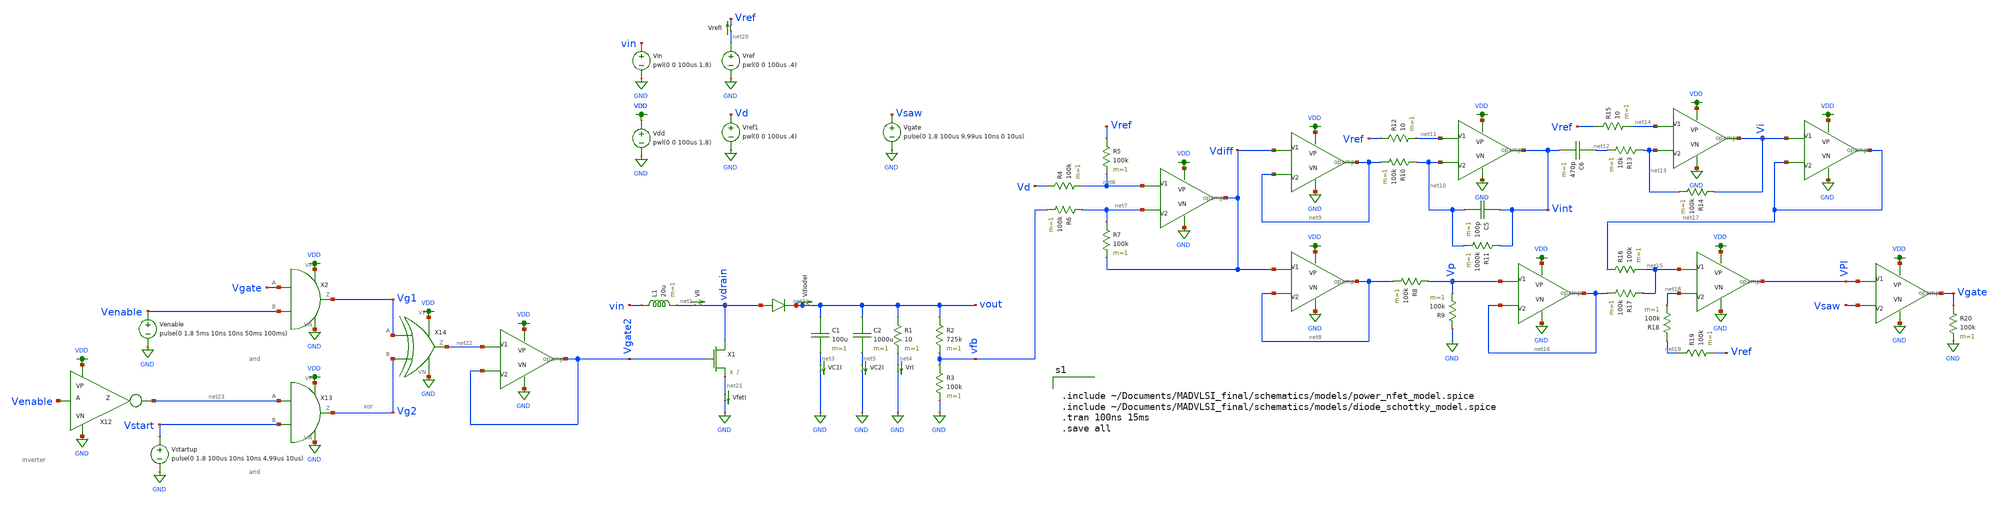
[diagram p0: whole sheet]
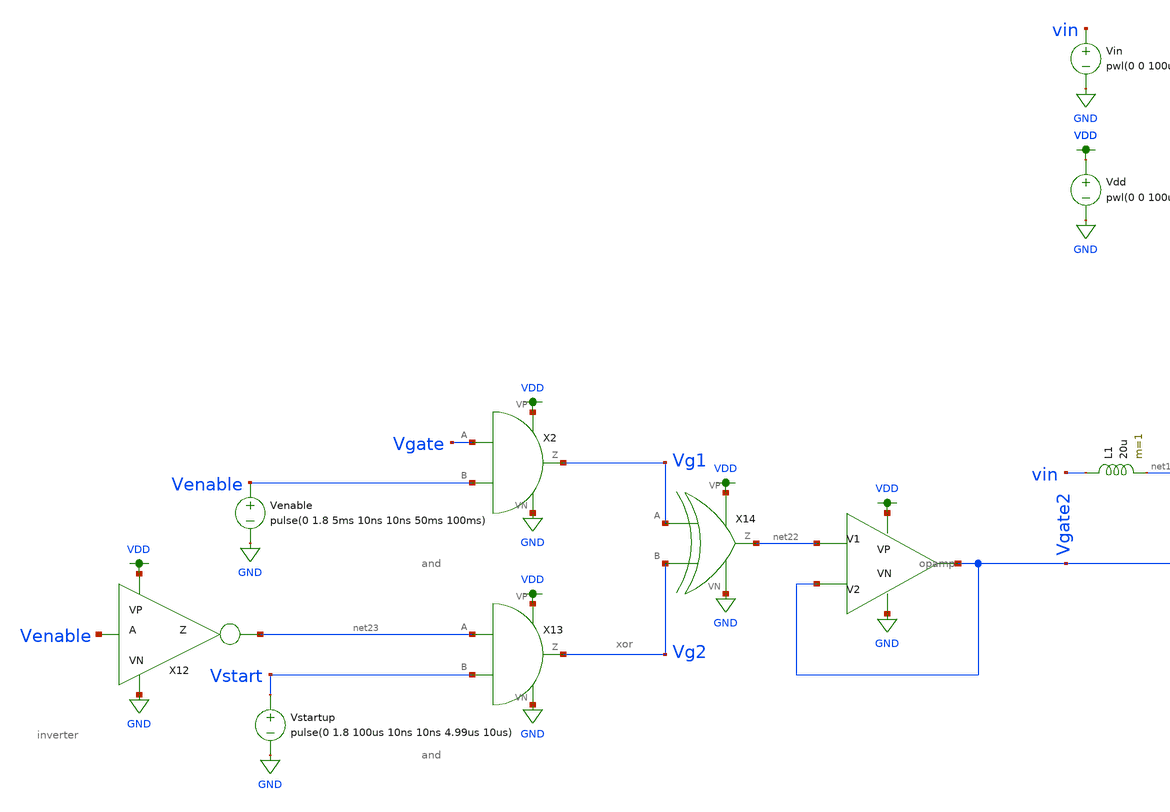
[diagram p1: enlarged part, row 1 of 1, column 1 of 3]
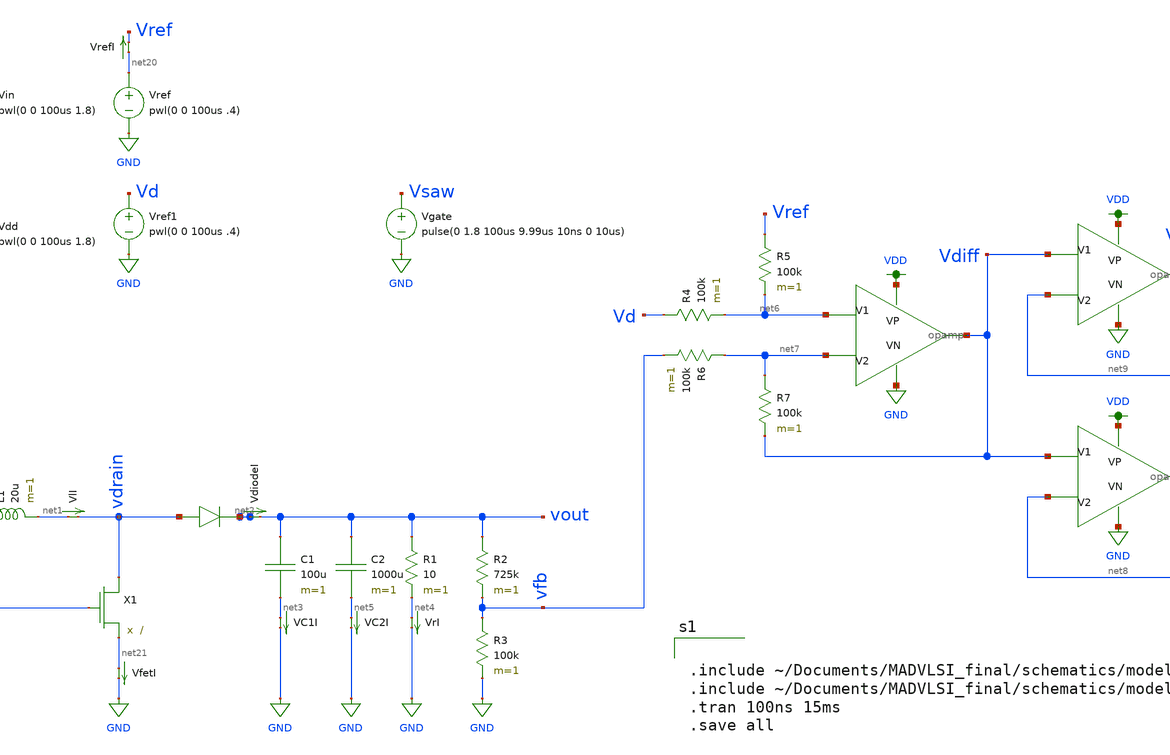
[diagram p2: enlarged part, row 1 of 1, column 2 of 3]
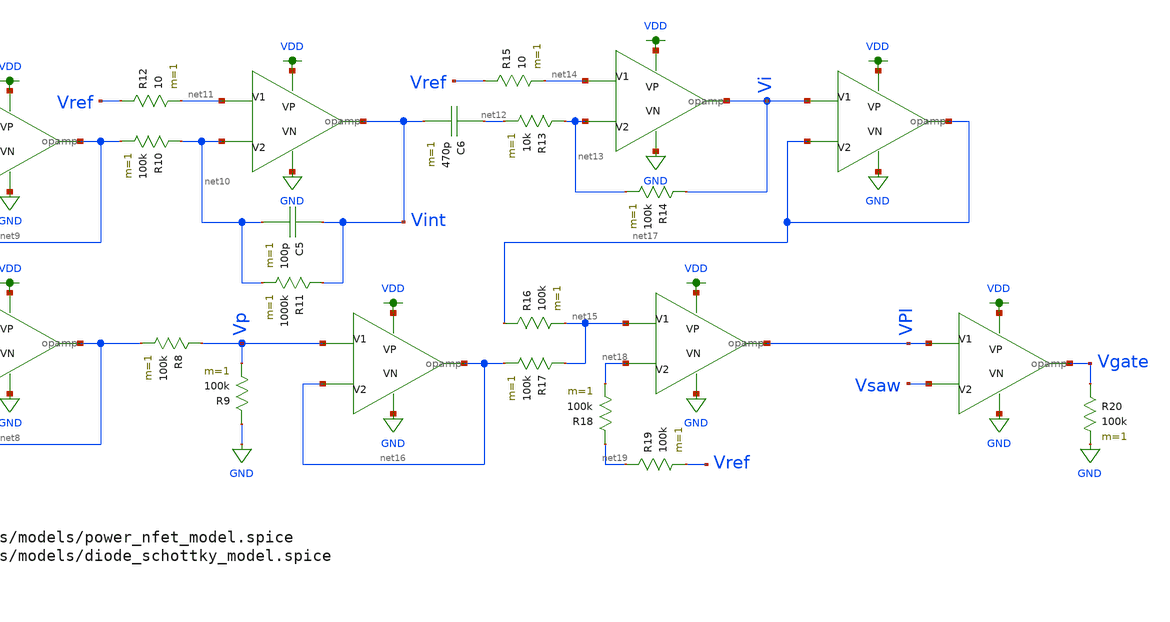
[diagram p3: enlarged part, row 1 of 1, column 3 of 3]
** sch_path: schematics/boost_VMC.sch
**.subckt boost_VMC
Vin vin GND pwl(0 0 100us 1.8)
VfetI net21 GND 0
.save i(vfeti)
X1 vdrain Vgate2 net21 power_nfet
L1 vin net1 20u m=1
D1 vdrain net2 diode_schottky
C1 vout net3 100u m=1
R1 vout net4 10 m=1
VlI net1 vdrain 0
.save i(vli)
VdiodeI net2 vout 0
.save i(vdiodei)
VC1I net3 GND 0
.save i(vc1i)
VrI net4 GND 0
.save i(vri)
C2 vout net5 1000u m=1
VC2I net5 GND 0
.save i(vc2i)
R2 vout vfb 725k m=1
R3 vfb GND 100k m=1
Vdd VDD GND pwl(0 0 100us 1.8)
Vref net20 GND pwl(0 0 100us .4)
R4 Vd net6 100k m=1
Vref1 Vd GND pwl(0 0 100us .4)
R5 Vref net6 100k m=1
R6 net7 vfb 100k m=1
R7 net7 Vdiff 100k m=1
X3 net6 net7 VDD GND Vdiff opamp
X4 Vdiff net8 VDD GND net8 opamp
X5 Vdiff net9 VDD GND net9 opamp
R8 Vp net8 100k m=1
R9 GND Vp 100k m=1
X6 net11 net10 VDD GND Vint opamp
R10 net10 net9 100k m=1
C5 Vint net10 100p m=1
R11 Vint net10 1000k m=1
R12 Vref net11 10 m=1
X7 net14 net13 VDD GND Vi opamp
C6 net12 Vint 470p m=1
R13 net13 net12 10k m=1
R14 Vi net13 100k m=1
R15 Vref net14 10 m=1
X8 net15 net18 VDD GND VPI opamp
R16 net17 net15 100k m=1
R17 net15 net16 100k m=1
X9 Vp net16 VDD GND net16 opamp
X10 Vi net17 VDD GND net17 opamp
R18 net19 net18 100k m=1
R19 net19 Vref 100k m=1
X11 VPI Vsaw VDD GND Vgate opamp
Vgate Vsaw GND pulse(0 1.8 100us 9.99us 10ns 0 10us)
VrefI net20 Vref 0
.save i(vrefi)
X2 Vgate Venable VDD GND Vg1 and
X12 Venable VDD GND net23 inverter
Venable Venable GND pulse(0 1.8 5ms 10ns 10ns 50ms 100ms)
R20 Vgate GND 100k m=1
X13 net23 Vstart VDD GND Vg2 and
Vstartup Vstart GND pulse(0 1.8 100us 10ns 10ns 4.99us 10us)
X14 Vg1 Vg2 VDD GND net22 xor
X15 net22 Vgate2 VDD GND Vgate2 opamp
**** begin user architecture code


.include ~/Documents/MADVLSI_final/schematics/models/power_nfet_model.spice
.include ~/Documents/MADVLSI_final/schematics/models/diode_schottky_model.spice
.tran 100ns 15ms
.save all


.option wnflag=1
.lib ~/skywater/skywater-pdk/libraries/sky130_fd_pr_ngspice/latest/models/sky130.lib.spice tt

**** end user architecture code
**.ends

* expanding   symbol:  /home/madvlsi/Documents/MADVLSI_final/schematics/opamp.sym # of pins=5
** sym_path: schematics/opamp.sym
** sch_path: schematics/opamp.sch
.subckt opamp V1 V2 VP VN Vout
*.ipin V1
*.ipin V2
*.opin Vout
*.iopin VP
*.iopin VN
*.iopin VP
*.iopin VN
XM1 VN net7 net2 GND sky130_fd_pr__nfet_01v8 L=l W=w nf=1 ad='int((nf+1)/2) * W/nf * 0.29' as='int((nf+2)/2) * W/nf * 0.29'
+ pd='2*int((nf+1)/2) * (W/nf + 0.29)' ps='2*int((nf+2)/2) * (W/nf + 0.29)' nrd='0.29 / W' nrs='0.29 / W'
+ sa=0 sb=0 sd=0 mult=1 m=1
XM2 VP net3 net1 VDD sky130_fd_pr__pfet_01v8 L=l W=w nf=1 ad='int((nf+1)/2) * W/nf * 0.29' as='int((nf+2)/2) * W/nf * 0.29'
+ pd='2*int((nf+1)/2) * (W/nf + 0.29)' ps='2*int((nf+2)/2) * (W/nf + 0.29)' nrd='0.29 / W' nrs='0.29 / W'
+ sa=0 sb=0 sd=0 mult=1 m=1
XM3 net1 V1 Vd VDD sky130_fd_pr__pfet_01v8 L=l W=w nf=1 ad='int((nf+1)/2) * W/nf * 0.29' as='int((nf+2)/2) * W/nf * 0.29'
+ pd='2*int((nf+1)/2) * (W/nf + 0.29)' ps='2*int((nf+2)/2) * (W/nf + 0.29)' nrd='0.29 / W' nrs='0.29 / W'
+ sa=0 sb=0 sd=0 mult=1 m=1
XM4 Vc V2 net1 VDD sky130_fd_pr__pfet_01v8 L=l W=w nf=1 ad='int((nf+1)/2) * W/nf * 0.29' as='int((nf+2)/2) * W/nf * 0.29'
+ pd='2*int((nf+1)/2) * (W/nf + 0.29)' ps='2*int((nf+2)/2) * (W/nf + 0.29)' nrd='0.29 / W' nrs='0.29 / W'
+ sa=0 sb=0 sd=0 mult=1 m=1
XM5 Va V2 net2 GND sky130_fd_pr__nfet_01v8 L=l W=w nf=1 ad='int((nf+1)/2) * W/nf * 0.29' as='int((nf+2)/2) * W/nf * 0.29'
+ pd='2*int((nf+1)/2) * (W/nf + 0.29)' ps='2*int((nf+2)/2) * (W/nf + 0.29)' nrd='0.29 / W' nrs='0.29 / W'
+ sa=0 sb=0 sd=0 mult=1 m=1
XM6 net2 V1 Vb GND sky130_fd_pr__nfet_01v8 L=l W=w nf=1 ad='int((nf+1)/2) * W/nf * 0.29' as='int((nf+2)/2) * W/nf * 0.29'
+ pd='2*int((nf+1)/2) * (W/nf + 0.29)' ps='2*int((nf+2)/2) * (W/nf + 0.29)' nrd='0.29 / W' nrs='0.29 / W'
+ sa=0 sb=0 sd=0 mult=1 m=1
XM7 net3 net3 Va VDD sky130_fd_pr__pfet_01v8 L=l W=w nf=1 ad='int((nf+1)/2) * W/nf * 0.29' as='int((nf+2)/2) * W/nf * 0.29'
+ pd='2*int((nf+1)/2) * (W/nf + 0.29)' ps='2*int((nf+2)/2) * (W/nf + 0.29)' nrd='0.29 / W' nrs='0.29 / W'
+ sa=0 sb=0 sd=0 mult=1 m=1
XM8 net6 net6 Va VDD sky130_fd_pr__pfet_01v8 L=l W=w nf=1 ad='int((nf+1)/2) * W/nf * 0.29' as='int((nf+2)/2) * W/nf * 0.29'
+ pd='2*int((nf+1)/2) * (W/nf + 0.29)' ps='2*int((nf+2)/2) * (W/nf + 0.29)' nrd='0.29 / W' nrs='0.29 / W'
+ sa=0 sb=0 sd=0 mult=1 m=1
XM9 net5 net6 Vb VDD sky130_fd_pr__pfet_01v8 L=l W=w nf=1 ad='int((nf+1)/2) * W/nf * 0.29' as='int((nf+2)/2) * W/nf * 0.29'
+ pd='2*int((nf+1)/2) * (W/nf + 0.29)' ps='2*int((nf+2)/2) * (W/nf + 0.29)' nrd='0.29 / W' nrs='0.29 / W'
+ sa=0 sb=0 sd=0 mult=1 m=1
XM10 Va net3 VP VDD sky130_fd_pr__pfet_01v8 L=l W=w nf=1 ad='int((nf+1)/2) * W/nf * 0.29' as='int((nf+2)/2) * W/nf * 0.29'
+ pd='2*int((nf+1)/2) * (W/nf + 0.29)' ps='2*int((nf+2)/2) * (W/nf + 0.29)' nrd='0.29 / W' nrs='0.29 / W'
+ sa=0 sb=0 sd=0 mult=1 m=1
XM11 Vb net3 VP VDD sky130_fd_pr__pfet_01v8 L=l W=w nf=1 ad='int((nf+1)/2) * W/nf * 0.29' as='int((nf+2)/2) * W/nf * 0.29'
+ pd='2*int((nf+1)/2) * (W/nf + 0.29)' ps='2*int((nf+2)/2) * (W/nf + 0.29)' nrd='0.29 / W' nrs='0.29 / W'
+ sa=0 sb=0 sd=0 mult=1 m=1
XM12 net6 net6 Vc GND sky130_fd_pr__nfet_01v8 L=l W=w nf=1 ad='int((nf+1)/2) * W/nf * 0.29' as='int((nf+2)/2) * W/nf * 0.29'
+ pd='2*int((nf+1)/2) * (W/nf + 0.29)' ps='2*int((nf+2)/2) * (W/nf + 0.29)' nrd='0.29 / W' nrs='0.29 / W'
+ sa=0 sb=0 sd=0 mult=1 m=1
XM13 net5 net6 Vd GND sky130_fd_pr__nfet_01v8 L=l W=w nf=1 ad='int((nf+1)/2) * W/nf * 0.29' as='int((nf+2)/2) * W/nf * 0.29'
+ pd='2*int((nf+1)/2) * (W/nf + 0.29)' ps='2*int((nf+2)/2) * (W/nf + 0.29)' nrd='0.29 / W' nrs='0.29 / W'
+ sa=0 sb=0 sd=0 mult=1 m=1
XM14 Vc net7 VN GND sky130_fd_pr__nfet_01v8 L=l W=w nf=1 ad='int((nf+1)/2) * W/nf * 0.29' as='int((nf+2)/2) * W/nf * 0.29'
+ pd='2*int((nf+1)/2) * (W/nf + 0.29)' ps='2*int((nf+2)/2) * (W/nf + 0.29)' nrd='0.29 / W' nrs='0.29 / W'
+ sa=0 sb=0 sd=0 mult=1 m=1
XM15 Vd net7 VN GND sky130_fd_pr__nfet_01v8 L=l W=w nf=1 ad='int((nf+1)/2) * W/nf * 0.29' as='int((nf+2)/2) * W/nf * 0.29'
+ pd='2*int((nf+1)/2) * (W/nf + 0.29)' ps='2*int((nf+2)/2) * (W/nf + 0.29)' nrd='0.29 / W' nrs='0.29 / W'
+ sa=0 sb=0 sd=0 mult=1 m=1
XM16 net8 net7 net3 GND sky130_fd_pr__nfet_01v8 L=l W=w nf=1 ad='int((nf+1)/2) * W/nf * 0.29' as='int((nf+2)/2) * W/nf * 0.29'
+ pd='2*int((nf+1)/2) * (W/nf + 0.29)' ps='2*int((nf+2)/2) * (W/nf + 0.29)' nrd='0.29 / W' nrs='0.29 / W'
+ sa=0 sb=0 sd=0 mult=1 m=1
XM17 VN net7 net8 GND sky130_fd_pr__nfet_01v8 L=l W=w nf=1 ad='int((nf+1)/2) * W/nf * 0.29' as='int((nf+2)/2) * W/nf * 0.29'
+ pd='2*int((nf+1)/2) * (W/nf + 0.29)' ps='2*int((nf+2)/2) * (W/nf + 0.29)' nrd='0.29 / W' nrs='0.29 / W'
+ sa=0 sb=0 sd=0 mult=1 m=1
XM18 net8 net7 VP GND sky130_fd_pr__nfet_01v8 L=l W=w nf=1 ad='int((nf+1)/2) * W/nf * 0.29' as='int((nf+2)/2) * W/nf * 0.29'
+ pd='2*int((nf+1)/2) * (W/nf + 0.29)' ps='2*int((nf+2)/2) * (W/nf + 0.29)' nrd='0.29 / W' nrs='0.29 / W'
+ sa=0 sb=0 sd=0 mult=M m=M
XM19 net4 net3 net7 VDD sky130_fd_pr__pfet_01v8 L=l W=w nf=1 ad='int((nf+1)/2) * W/nf * 0.29' as='int((nf+2)/2) * W/nf * 0.29'
+ pd='2*int((nf+1)/2) * (W/nf + 0.29)' ps='2*int((nf+2)/2) * (W/nf + 0.29)' nrd='0.29 / W' nrs='0.29 / W'
+ sa=0 sb=0 sd=0 mult=1 m=1
XM20 VP net3 net4 VDD sky130_fd_pr__pfet_01v8 L=l W=w nf=1 ad='int((nf+1)/2) * W/nf * 0.29' as='int((nf+2)/2) * W/nf * 0.29'
+ pd='2*int((nf+1)/2) * (W/nf + 0.29)' ps='2*int((nf+2)/2) * (W/nf + 0.29)' nrd='0.29 / W' nrs='0.29 / W'
+ sa=0 sb=0 sd=0 mult=1 m=1
XM21 net4 net3 VN VDD sky130_fd_pr__pfet_01v8 L=l W=w nf=1 ad='int((nf+1)/2) * W/nf * 0.29' as='int((nf+2)/2) * W/nf * 0.29'
+ pd='2*int((nf+1)/2) * (W/nf + 0.29)' ps='2*int((nf+2)/2) * (W/nf + 0.29)' nrd='0.29 / W' nrs='0.29 / W'
+ sa=0 sb=0 sd=0 mult=M m=M
XM22 net7 net7 Vc GND sky130_fd_pr__nfet_01v8 L=l W=w nf=1 ad='int((nf+1)/2) * W/nf * 0.29' as='int((nf+2)/2) * W/nf * 0.29'
+ pd='2*int((nf+1)/2) * (W/nf + 0.29)' ps='2*int((nf+2)/2) * (W/nf + 0.29)' nrd='0.29 / W' nrs='0.29 / W'
+ sa=0 sb=0 sd=0 mult=1 m=1
**** begin user architecture code

.param M=3
.param w=3
.param l=0.6


**** end user architecture code
XM23 Vout net5 VN GND sky130_fd_pr__nfet_01v8 L=.15 W=6 nf=1 ad='int((nf+1)/2) * W/nf * 0.29' as='int((nf+2)/2) * W/nf * 0.29'
+ pd='2*int((nf+1)/2) * (W/nf + 0.29)' ps='2*int((nf+2)/2) * (W/nf + 0.29)' nrd='0.29 / W' nrs='0.29 / W'
+ sa=0 sb=0 sd=0 mult=1 m=1
XM24 Vout net5 VP VDD sky130_fd_pr__pfet_01v8 L=.15 W=12 nf=1 ad='int((nf+1)/2) * W/nf * 0.29' as='int((nf+2)/2) * W/nf * 0.29'
+ pd='2*int((nf+1)/2) * (W/nf + 0.29)' ps='2*int((nf+2)/2) * (W/nf + 0.29)' nrd='0.29 / W' nrs='0.29 / W'
+ sa=0 sb=0 sd=0 mult=1 m=1
C1 Vout net5 500f m=1
.ends


* expanding   symbol:  /home/madvlsi/Documents/MADVLSI_final/schematics/and.sym # of pins=6
** sym_path: schematics/and.sym
** sch_path: schematics/and.sch
.subckt and A B VP VN Z
*.ipin A
*.ipin B
*.iopin VP
*.iopin VN
*.opin Z
X1 net1 VP VN Z inverter
X2 A B VP VN net1 nand
**** begin user architecture code

.param l=.15
.param w=1
.param mn=1
.param mp=1

**** end user architecture code
.ends


* expanding   symbol:  /home/madvlsi/Documents/MADVLSI_final/schematics/inverter.sym # of pins=4
** sym_path: schematics/inverter.sym
** sch_path: schematics/inverter.sch
.subckt inverter A VP VN Z
*.ipin A
*.iopin VP
*.iopin VN
*.opin Z
XM1 Z A VN GND sky130_fd_pr__nfet_01v8 L=0.15 W=1 nf=1 ad='int((nf+1)/2) * W/nf * 0.29' as='int((nf+2)/2) * W/nf * 0.29'
+ pd='2*int((nf+1)/2) * (W/nf + 0.29)' ps='2*int((nf+2)/2) * (W/nf + 0.29)' nrd='0.29 / W' nrs='0.29 / W'
+ sa=0 sb=0 sd=0 mult=1 m=1
XM2 Z A VP VDD sky130_fd_pr__pfet_01v8 L=0.15 W=1 nf=1 ad='int((nf+1)/2) * W/nf * 0.29' as='int((nf+2)/2) * W/nf * 0.29'
+ pd='2*int((nf+1)/2) * (W/nf + 0.29)' ps='2*int((nf+2)/2) * (W/nf + 0.29)' nrd='0.29 / W' nrs='0.29 / W'
+ sa=0 sb=0 sd=0 mult=2 m=2
**** begin user architecture code

.param l=.15
.param w=1
.param mn=1
.param mp=1

**** end user architecture code
.ends


* expanding   symbol:  /home/madvlsi/Documents/MADVLSI_final/schematics/xor.sym # of pins=6
** sym_path: schematics/xor.sym
** sch_path: schematics/xor.sch
.subckt xor A B VP VN Z
*.ipin A
*.ipin B
*.iopin VP
*.iopin VN
*.opin Z
X1 A B VP VN net1 nand
X2 net1 B VP VN net2 nand
X3 A net1 VP VN net3 nand
X4 net3 net2 VP VN Z nand
**** begin user architecture code

.param l=.15
.param w=1
.param mn=1
.param mp=1

**** end user architecture code
.ends


* expanding   symbol:  /home/madvlsi/Documents/final/xschem/nand.sym # of pins=6
** sym_path: schematics/nand.sym
** sch_path: schematics/nand.sch
.subckt nand A B VP VN Z
*.ipin A
*.iopin VP
*.iopin VN
*.opin Z
*.ipin B
XM1 Z A net1 GND sky130_fd_pr__nfet_01v8 L=0.15 W=1 nf=1 ad='int((nf+1)/2) * W/nf * 0.29' as='int((nf+2)/2) * W/nf * 0.29'
+ pd='2*int((nf+1)/2) * (W/nf + 0.29)' ps='2*int((nf+2)/2) * (W/nf + 0.29)' nrd='0.29 / W' nrs='0.29 / W'
+ sa=0 sb=0 sd=0 mult=1 m=1
XM2 VP B Z VDD sky130_fd_pr__pfet_01v8 L=0.15 W=1 nf=1 ad='int((nf+1)/2) * W/nf * 0.29' as='int((nf+2)/2) * W/nf * 0.29'
+ pd='2*int((nf+1)/2) * (W/nf + 0.29)' ps='2*int((nf+2)/2) * (W/nf + 0.29)' nrd='0.29 / W' nrs='0.29 / W'
+ sa=0 sb=0 sd=0 mult=2 m=2
XM3 VN B net1 GND sky130_fd_pr__nfet_01v8 L=0.15 W=1 nf=1 ad='int((nf+1)/2) * W/nf * 0.29' as='int((nf+2)/2) * W/nf * 0.29'
+ pd='2*int((nf+1)/2) * (W/nf + 0.29)' ps='2*int((nf+2)/2) * (W/nf + 0.29)' nrd='0.29 / W' nrs='0.29 / W'
+ sa=0 sb=0 sd=0 mult=1 m=1
XM4 Z A VP VDD sky130_fd_pr__pfet_01v8 L=0.15 W=1 nf=1 ad='int((nf+1)/2) * W/nf * 0.29' as='int((nf+2)/2) * W/nf * 0.29'
+ pd='2*int((nf+1)/2) * (W/nf + 0.29)' ps='2*int((nf+2)/2) * (W/nf + 0.29)' nrd='0.29 / W' nrs='0.29 / W'
+ sa=0 sb=0 sd=0 mult=2 m=2
.ends

.GLOBAL GND
.GLOBAL VDD
.end
